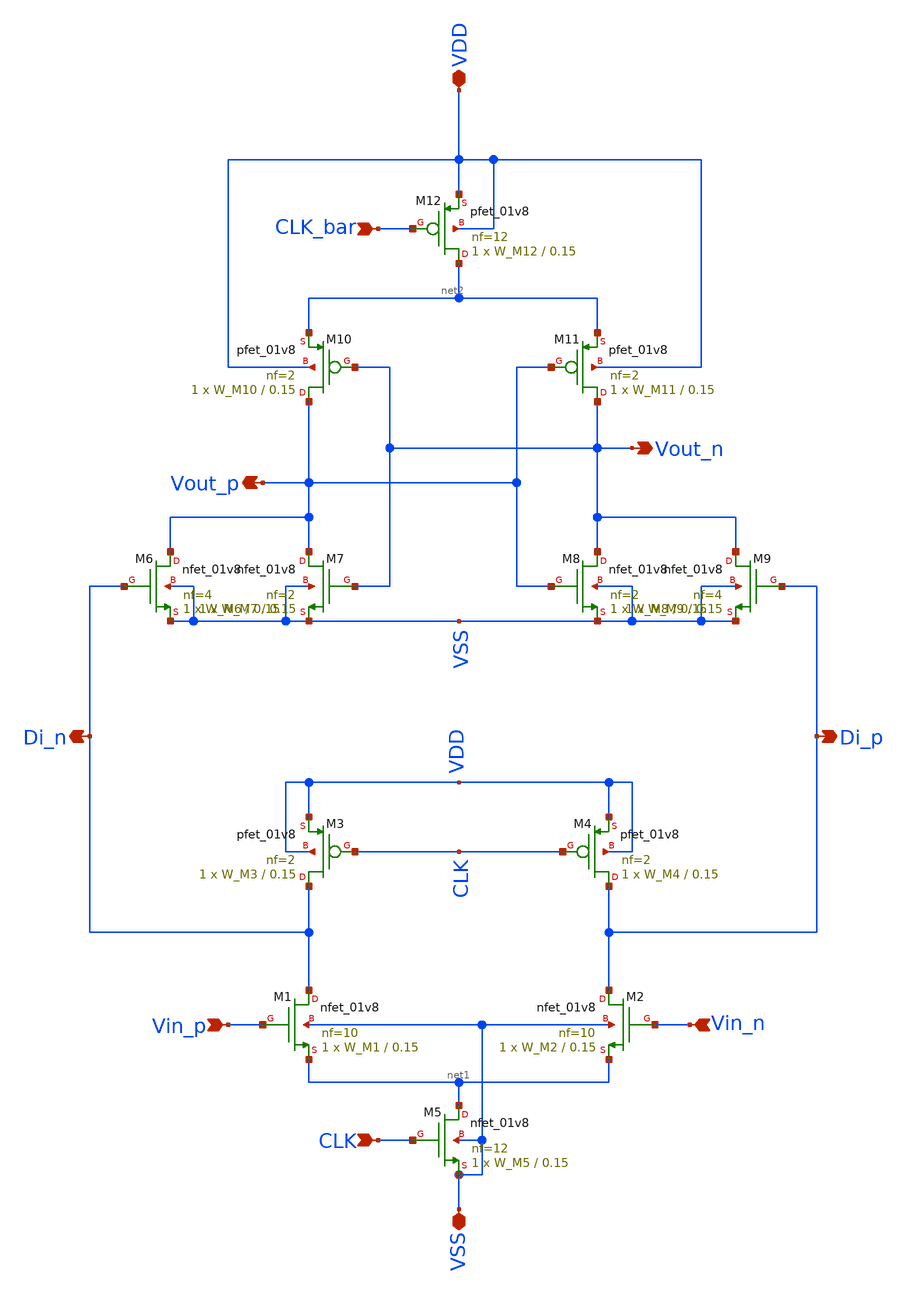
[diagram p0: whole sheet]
** sch_path: xschem/double_tail_comp.sch
**.subckt double_tail_comp CLK Vin_p Vin_n Di_n Di_p Vout_n Vout_p CLK_bar VDD VSS
*.ipin CLK
*.ipin Vin_p
*.ipin Vin_n
*.opin Di_n
*.opin Di_p
*.opin Vout_n
*.opin Vout_p
*.ipin CLK_bar
*.iopin VDD
*.iopin VSS
XM1 Di_n Vin_p net1 VSS sky130_fd_pr__nfet_01v8 L=0.15 W=W_M1 nf=10 ad='int((nf+1)/2) * W/nf * 0.29'
+ as='int((nf+2)/2) * W/nf * 0.29' pd='2*int((nf+1)/2) * (W/nf + 0.29)' ps='2*int((nf+2)/2) * (W/nf + 0.29)'
+ nrd='0.29 / W' nrs='0.29 / W' sa=0 sb=0 sd=0 mult=1 m=1
XM2 Di_p Vin_n net1 VSS sky130_fd_pr__nfet_01v8 L=0.15 W=W_M2 nf=10 ad='int((nf+1)/2) * W/nf * 0.29'
+ as='int((nf+2)/2) * W/nf * 0.29' pd='2*int((nf+1)/2) * (W/nf + 0.29)' ps='2*int((nf+2)/2) * (W/nf + 0.29)'
+ nrd='0.29 / W' nrs='0.29 / W' sa=0 sb=0 sd=0 mult=1 m=1
XM3 Di_n CLK VDD VDD sky130_fd_pr__pfet_01v8 L=0.15 W=W_M3 nf=2 ad='int((nf+1)/2) * W/nf * 0.29' as='int((nf+2)/2) * W/nf * 0.29'
+ pd='2*int((nf+1)/2) * (W/nf + 0.29)' ps='2*int((nf+2)/2) * (W/nf + 0.29)' nrd='0.29 / W' nrs='0.29 / W'
+ sa=0 sb=0 sd=0 mult=1 m=1
XM4 Di_p CLK VDD VDD sky130_fd_pr__pfet_01v8 L=0.15 W=W_M4 nf=2 ad='int((nf+1)/2) * W/nf * 0.29' as='int((nf+2)/2) * W/nf * 0.29'
+ pd='2*int((nf+1)/2) * (W/nf + 0.29)' ps='2*int((nf+2)/2) * (W/nf + 0.29)' nrd='0.29 / W' nrs='0.29 / W'
+ sa=0 sb=0 sd=0 mult=1 m=1
XM5 net1 CLK VSS VSS sky130_fd_pr__nfet_01v8 L=0.15 W=W_M5 nf=12 ad='int((nf+1)/2) * W/nf * 0.29' as='int((nf+2)/2) * W/nf * 0.29'
+ pd='2*int((nf+1)/2) * (W/nf + 0.29)' ps='2*int((nf+2)/2) * (W/nf + 0.29)' nrd='0.29 / W' nrs='0.29 / W'
+ sa=0 sb=0 sd=0 mult=1 m=1
XM6 Vout_p Di_n VSS VSS sky130_fd_pr__nfet_01v8 L=0.15 W=W_M6 nf=4 ad='int((nf+1)/2) * W/nf * 0.29' as='int((nf+2)/2) * W/nf * 0.29'
+ pd='2*int((nf+1)/2) * (W/nf + 0.29)' ps='2*int((nf+2)/2) * (W/nf + 0.29)' nrd='0.29 / W' nrs='0.29 / W'
+ sa=0 sb=0 sd=0 mult=1 m=1
XM7 Vout_p Vout_n VSS VSS sky130_fd_pr__nfet_01v8 L=0.15 W=W_M7 nf=2 ad='int((nf+1)/2) * W/nf * 0.29'
+ as='int((nf+2)/2) * W/nf * 0.29' pd='2*int((nf+1)/2) * (W/nf + 0.29)' ps='2*int((nf+2)/2) * (W/nf + 0.29)'
+ nrd='0.29 / W' nrs='0.29 / W' sa=0 sb=0 sd=0 mult=1 m=1
XM8 Vout_n Vout_p VSS VSS sky130_fd_pr__nfet_01v8 L=0.15 W=W_M8 nf=2 ad='int((nf+1)/2) * W/nf * 0.29'
+ as='int((nf+2)/2) * W/nf * 0.29' pd='2*int((nf+1)/2) * (W/nf + 0.29)' ps='2*int((nf+2)/2) * (W/nf + 0.29)'
+ nrd='0.29 / W' nrs='0.29 / W' sa=0 sb=0 sd=0 mult=1 m=1
XM9 Vout_n Di_p VSS VSS sky130_fd_pr__nfet_01v8 L=0.15 W=W_M9 nf=4 ad='int((nf+1)/2) * W/nf * 0.29' as='int((nf+2)/2) * W/nf * 0.29'
+ pd='2*int((nf+1)/2) * (W/nf + 0.29)' ps='2*int((nf+2)/2) * (W/nf + 0.29)' nrd='0.29 / W' nrs='0.29 / W'
+ sa=0 sb=0 sd=0 mult=1 m=1
XM10 Vout_p Vout_n net2 VDD sky130_fd_pr__pfet_01v8 L=0.15 W=W_M10 nf=2 ad='int((nf+1)/2) * W/nf * 0.29'
+ as='int((nf+2)/2) * W/nf * 0.29' pd='2*int((nf+1)/2) * (W/nf + 0.29)' ps='2*int((nf+2)/2) * (W/nf + 0.29)'
+ nrd='0.29 / W' nrs='0.29 / W' sa=0 sb=0 sd=0 mult=1 m=1
XM11 Vout_n Vout_p net2 VDD sky130_fd_pr__pfet_01v8 L=0.15 W=W_M11 nf=2 ad='int((nf+1)/2) * W/nf * 0.29'
+ as='int((nf+2)/2) * W/nf * 0.29' pd='2*int((nf+1)/2) * (W/nf + 0.29)' ps='2*int((nf+2)/2) * (W/nf + 0.29)'
+ nrd='0.29 / W' nrs='0.29 / W' sa=0 sb=0 sd=0 mult=1 m=1
XM12 net2 CLK_bar VDD VDD sky130_fd_pr__pfet_01v8 L=0.15 W=W_M12 nf=12 ad='int((nf+1)/2) * W/nf * 0.29'
+ as='int((nf+2)/2) * W/nf * 0.29' pd='2*int((nf+1)/2) * (W/nf + 0.29)' ps='2*int((nf+2)/2) * (W/nf + 0.29)'
+ nrd='0.29 / W' nrs='0.29 / W' sa=0 sb=0 sd=0 mult=1 m=1
**.ends
.end
